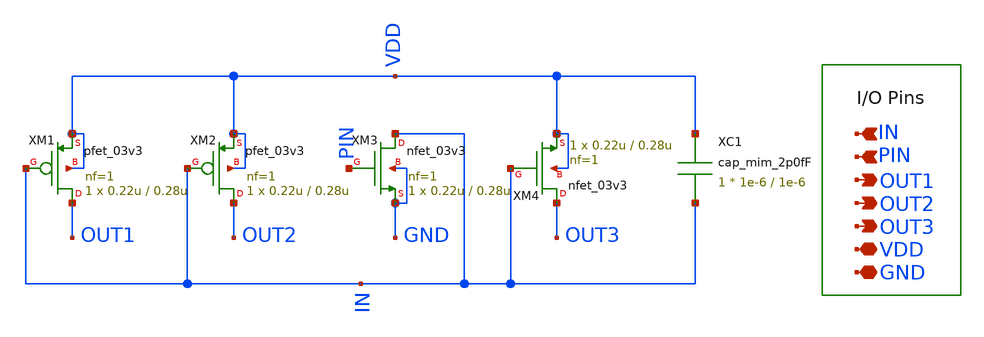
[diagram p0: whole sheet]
** sch_path: gf180_current_3_mirror-ckt.sch
**.subckt gf180_current_3_mirror-ckt IN OUT2 VDD GND OUT3 OUT1 PIN
*.ipin IN
*.opin OUT2
*.iopin VDD
*.iopin GND
*.opin OUT3
*.opin OUT1
*.ipin PIN
XM1 OUT1 IN VDD VDD pfet_03v3 L=0.28u W=0.22u nf=1 ad='int((nf+1)/2) * W/nf * 0.18u' as='int((nf+2)/2) * W/nf * 0.18u'
+ pd='2*int((nf+1)/2) * (W/nf + 0.18u)' ps='2*int((nf+2)/2) * (W/nf + 0.18u)' nrd='0.18u / W' nrs='0.18u / W'
+ sa=0 sb=0 sd=0 m=1
XM2 OUT2 IN VDD VDD pfet_03v3 L=0.28u W=0.22u nf=1 ad='int((nf+1)/2) * W/nf * 0.18u' as='int((nf+2)/2) * W/nf * 0.18u'
+ pd='2*int((nf+1)/2) * (W/nf + 0.18u)' ps='2*int((nf+2)/2) * (W/nf + 0.18u)' nrd='0.18u / W' nrs='0.18u / W'
+ sa=0 sb=0 sd=0 m=1
XM3 IN PIN GND GND nfet_03v3 L=0.28u W=0.22u nf=1 ad='int((nf+1)/2) * W/nf * 0.18u' as='int((nf+2)/2) * W/nf * 0.18u'
+ pd='2*int((nf+1)/2) * (W/nf + 0.18u)' ps='2*int((nf+2)/2) * (W/nf + 0.18u)' nrd='0.18u / W' nrs='0.18u / W'
+ sa=0 sb=0 sd=0 m=1
XM4 OUT3 IN VDD VDD nfet_03v3 L=0.28u W=0.22u nf=1 ad='int((nf+1)/2) * W/nf * 0.18u' as='int((nf+2)/2) * W/nf * 0.18u'
+ pd='2*int((nf+1)/2) * (W/nf + 0.18u)' ps='2*int((nf+2)/2) * (W/nf + 0.18u)' nrd='0.18u / W' nrs='0.18u / W'
+ sa=0 sb=0 sd=0 m=1
XC1 VDD IN cap_mim_2p0fF c_width=1e-6 c_length=1e-6 m=1
**.ends
.end
